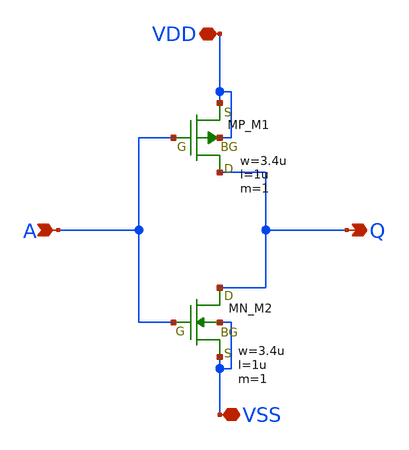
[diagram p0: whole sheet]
** sch_path: samples/inverter/OpenSUSI-TR10/inverter.sch
**.subckt inverter A Q VDD VSS
*.ipin A
*.opin Q
*.iopin VDD
*.iopin VSS
XM1 Q A VDD VDD PMOS w=3.4u l=1u as=0 ad=0 ps=0 pd=0 nrd=0 nrs=0 m=1
XM2 Q A VSS VSS NMOS w=3.4u l=1u as=0 ad=0 ps=0 pd=0 nrd=0 nrs=0 m=1
**.ends
.end
